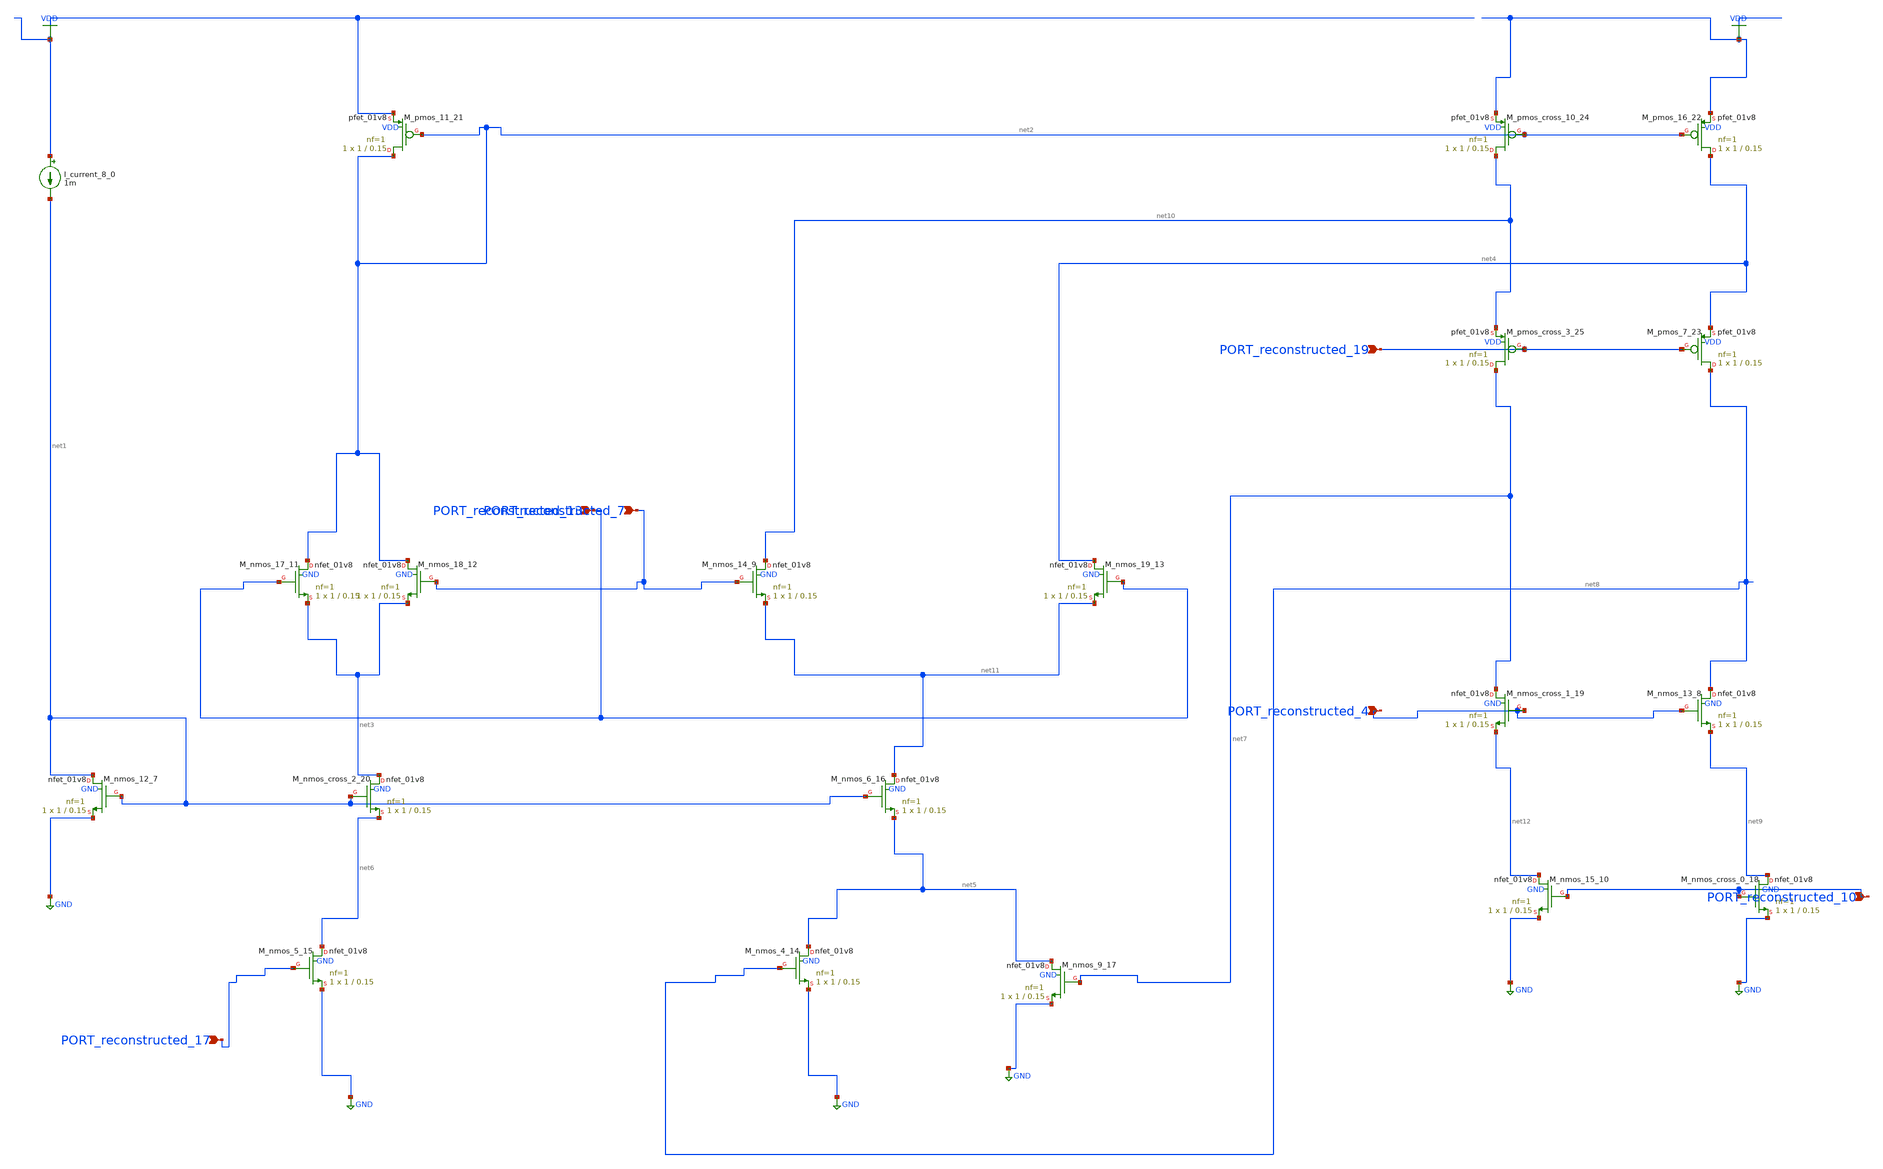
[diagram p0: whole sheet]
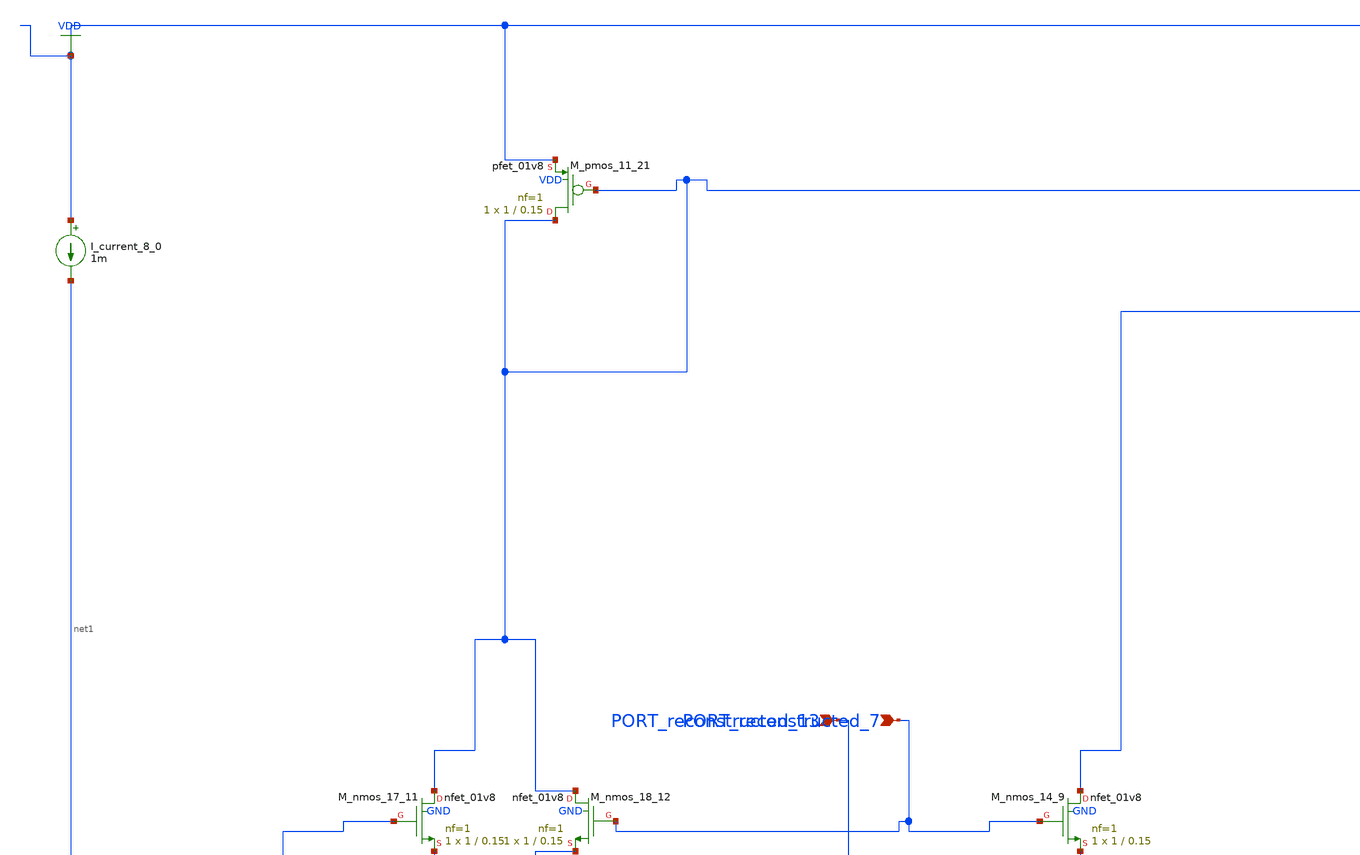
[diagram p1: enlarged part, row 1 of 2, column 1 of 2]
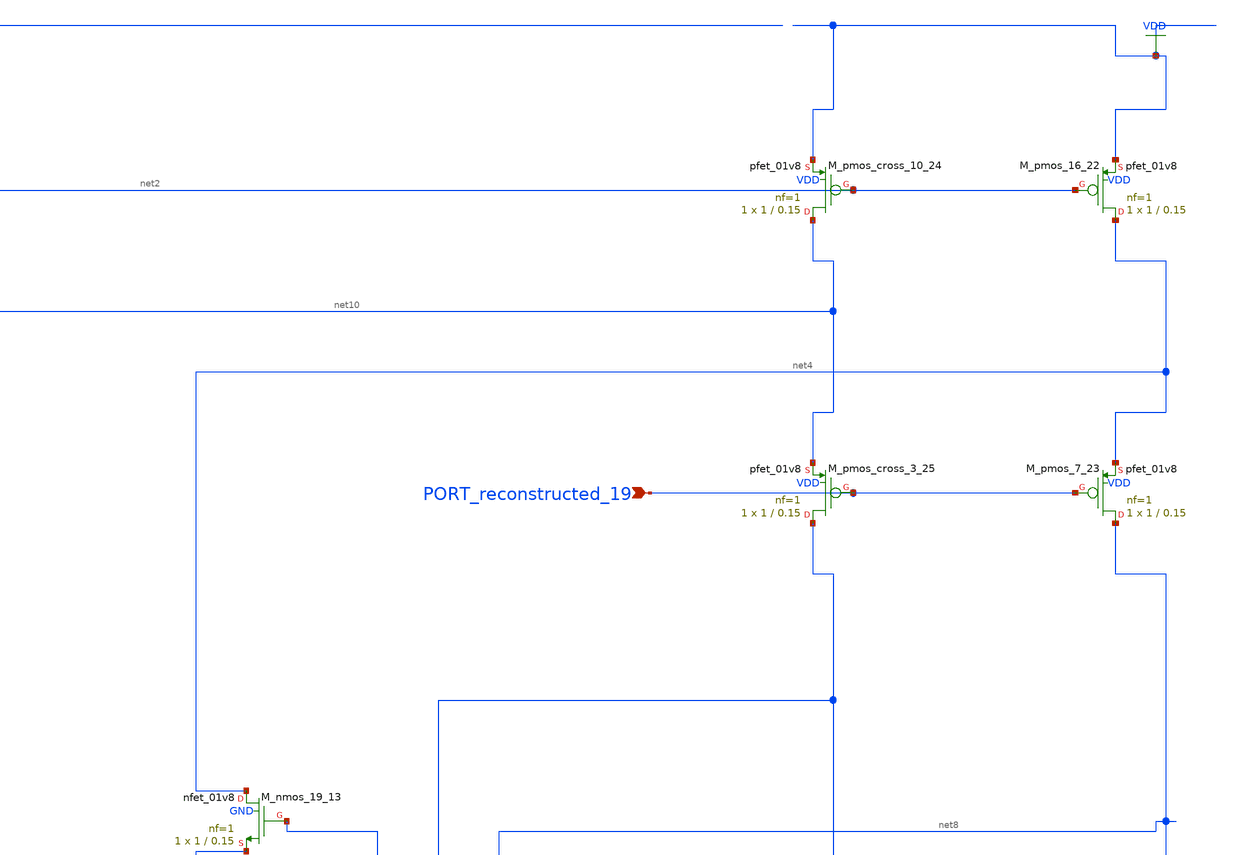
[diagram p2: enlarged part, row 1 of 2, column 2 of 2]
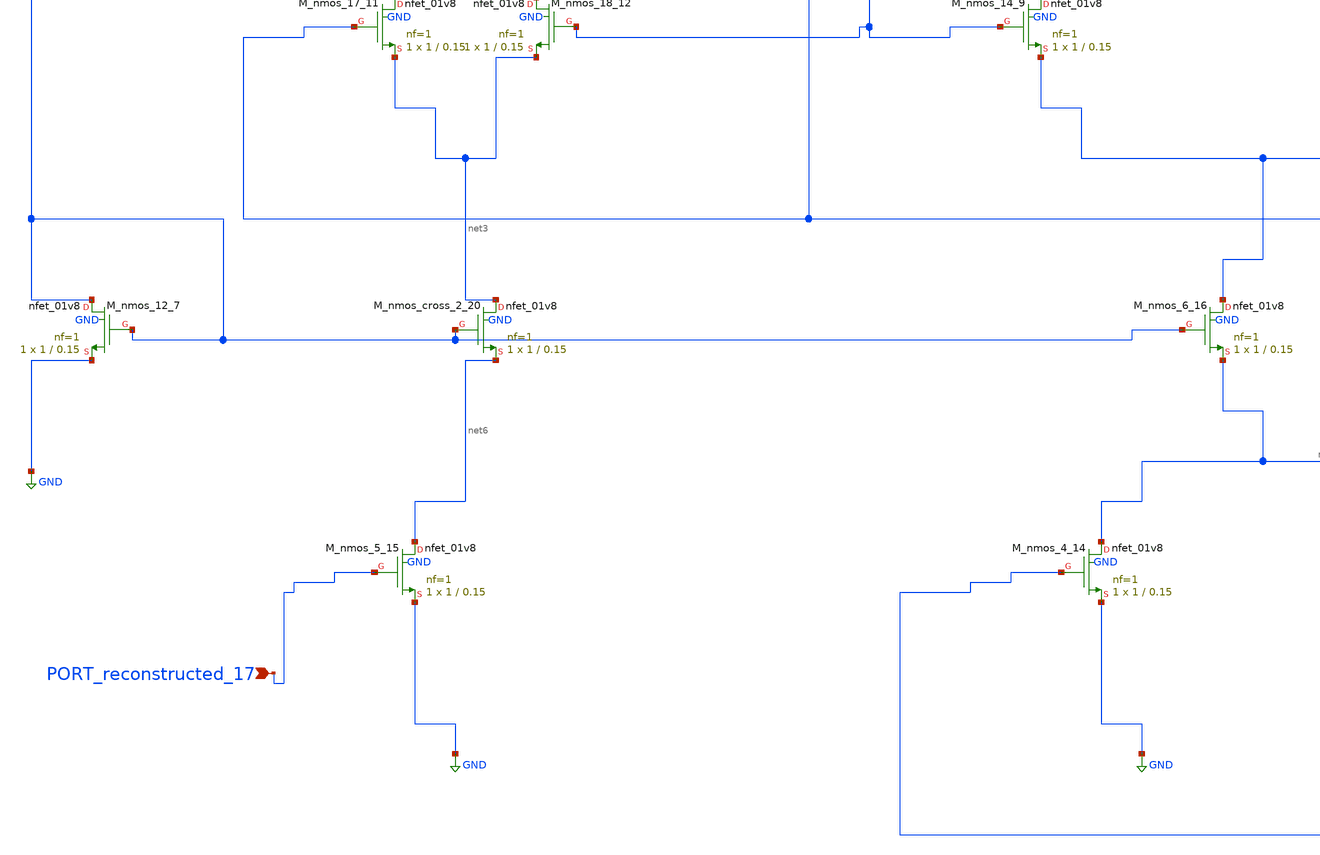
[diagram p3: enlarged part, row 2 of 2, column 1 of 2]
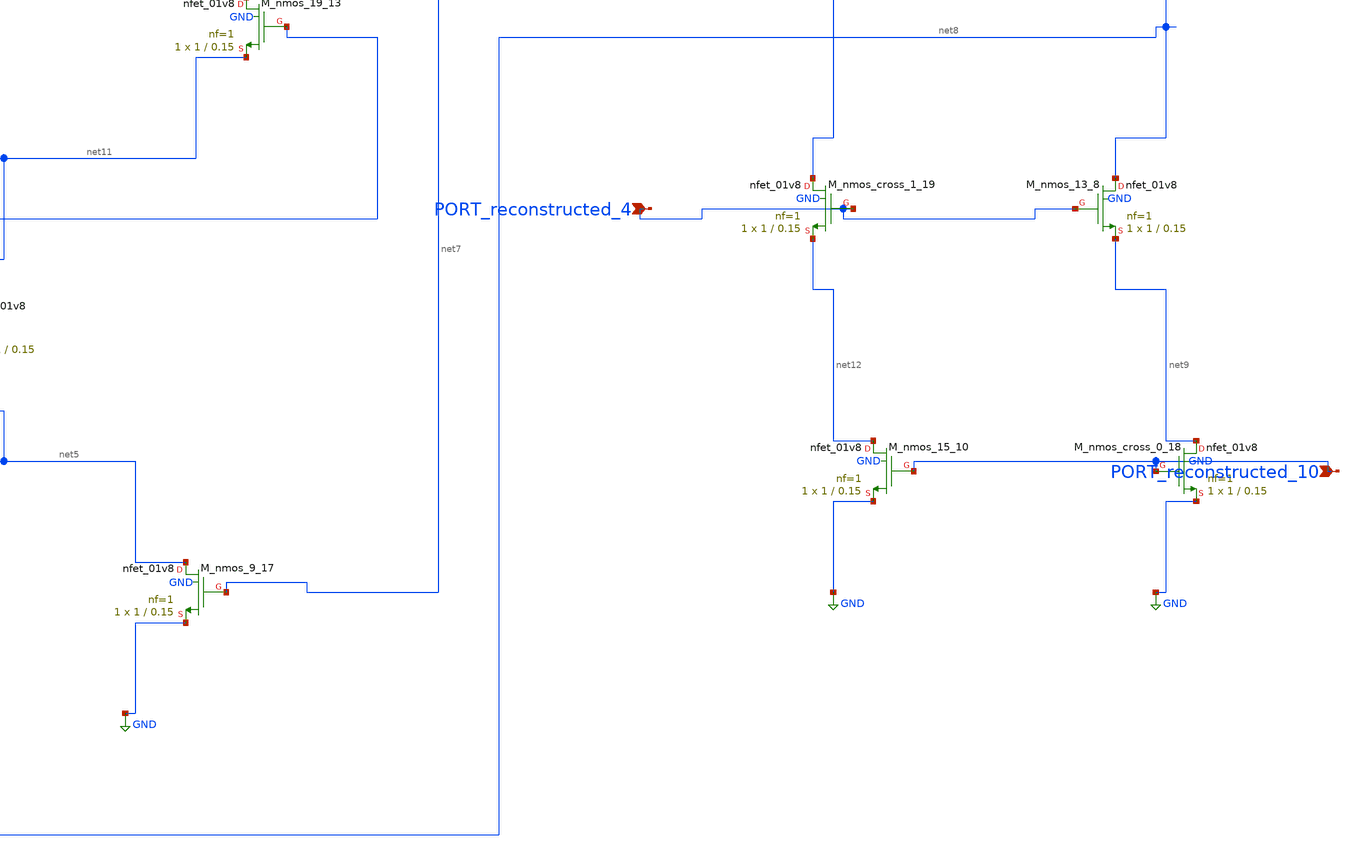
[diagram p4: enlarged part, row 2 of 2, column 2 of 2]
** sch_path: schematics/AMSNet/673.sch
**.subckt 673 PORT_reconstructed_7 PORT_reconstructed_13 PORT_reconstructed_17 PORT_reconstructed_10
*+ PORT_reconstructed_4 PORT_reconstructed_19
*.ipin PORT_reconstructed_7
*.ipin PORT_reconstructed_13
*.ipin PORT_reconstructed_17
*.ipin PORT_reconstructed_10
*.ipin PORT_reconstructed_4
*.ipin PORT_reconstructed_19
I_current_8_0 VDD net1 1m
XM_nmos_12_7 net1 net1 GND GND sky130_fd_pr__nfet_01v8 L=0.15 W=1 nf=1 ad='int((1 + 1)/2) * 1 / 1 * 0.29'
+ as='int((1 + 2)/2) * 1 / 1 * 0.29' pd='2*int((1 + 1)/2) * (1 / 1 + 0.29)' ps='2*int((1 + 2)/2) * (1 / 1 + 0.29)'
+ nrd='0.29 / 1 ' nrs='0.29 / 1 ' sa=0 sb=0 sd=0 mult=1 m=1
XM_nmos_13_8 net8 PORT_reconstructed_4 net9 GND sky130_fd_pr__nfet_01v8 L=0.15 W=1 nf=1 ad='int((1 + 1)/2) * 1 / 1 * 0.29'
+ as='int((1 + 2)/2) * 1 / 1 * 0.29' pd='2*int((1 + 1)/2) * (1 / 1 + 0.29)' ps='2*int((1 + 2)/2) * (1 / 1 + 0.29)'
+ nrd='0.29 / 1 ' nrs='0.29 / 1 ' sa=0 sb=0 sd=0 mult=1 m=1
XM_nmos_14_9 net10 PORT_reconstructed_7 net11 GND sky130_fd_pr__nfet_01v8 L=0.15 W=1 nf=1 ad='int((1 + 1)/2) * 1 / 1 * 0.29'
+ as='int((1 + 2)/2) * 1 / 1 * 0.29' pd='2*int((1 + 1)/2) * (1 / 1 + 0.29)' ps='2*int((1 + 2)/2) * (1 / 1 + 0.29)'
+ nrd='0.29 / 1 ' nrs='0.29 / 1 ' sa=0 sb=0 sd=0 mult=1 m=1
XM_nmos_15_10 net12 PORT_reconstructed_10 GND GND sky130_fd_pr__nfet_01v8 L=0.15 W=1 nf=1 ad='int((1 + 1)/2) * 1 / 1 * 0.29'
+ as='int((1 + 2)/2) * 1 / 1 * 0.29' pd='2*int((1 + 1)/2) * (1 / 1 + 0.29)' ps='2*int((1 + 2)/2) * (1 / 1 + 0.29)'
+ nrd='0.29 / 1 ' nrs='0.29 / 1 ' sa=0 sb=0 sd=0 mult=1 m=1
XM_nmos_17_11 net2 PORT_reconstructed_13 net3 GND sky130_fd_pr__nfet_01v8 L=0.15 W=1 nf=1 ad='int((1 + 1)/2) * 1 / 1 * 0.29'
+ as='int((1 + 2)/2) * 1 / 1 * 0.29' pd='2*int((1 + 1)/2) * (1 / 1 + 0.29)' ps='2*int((1 + 2)/2) * (1 / 1 + 0.29)'
+ nrd='0.29 / 1 ' nrs='0.29 / 1 ' sa=0 sb=0 sd=0 mult=1 m=1
XM_nmos_18_12 net2 PORT_reconstructed_7 net3 GND sky130_fd_pr__nfet_01v8 L=0.15 W=1 nf=1 ad='int((1 + 1)/2) * 1 / 1 * 0.29'
+ as='int((1 + 2)/2) * 1 / 1 * 0.29' pd='2*int((1 + 1)/2) * (1 / 1 + 0.29)' ps='2*int((1 + 2)/2) * (1 / 1 + 0.29)'
+ nrd='0.29 / 1 ' nrs='0.29 / 1 ' sa=0 sb=0 sd=0 mult=1 m=1
XM_nmos_19_13 net4 PORT_reconstructed_13 net11 GND sky130_fd_pr__nfet_01v8 L=0.15 W=1 nf=1 ad='int((1 + 1)/2) * 1 / 1 * 0.29'
+ as='int((1 + 2)/2) * 1 / 1 * 0.29' pd='2*int((1 + 1)/2) * (1 / 1 + 0.29)' ps='2*int((1 + 2)/2) * (1 / 1 + 0.29)'
+ nrd='0.29 / 1 ' nrs='0.29 / 1 ' sa=0 sb=0 sd=0 mult=1 m=1
XM_nmos_4_14 net5 net8 GND GND sky130_fd_pr__nfet_01v8 L=0.15 W=1 nf=1 ad='int((1 + 1)/2) * 1 / 1 * 0.29'
+ as='int((1 + 2)/2) * 1 / 1 * 0.29' pd='2*int((1 + 1)/2) * (1 / 1 + 0.29)' ps='2*int((1 + 2)/2) * (1 / 1 + 0.29)'
+ nrd='0.29 / 1 ' nrs='0.29 / 1 ' sa=0 sb=0 sd=0 mult=1 m=1
XM_nmos_5_15 net6 PORT_reconstructed_17 GND GND sky130_fd_pr__nfet_01v8 L=0.15 W=1 nf=1 ad='int((1 + 1)/2) * 1 / 1 * 0.29'
+ as='int((1 + 2)/2) * 1 / 1 * 0.29' pd='2*int((1 + 1)/2) * (1 / 1 + 0.29)' ps='2*int((1 + 2)/2) * (1 / 1 + 0.29)'
+ nrd='0.29 / 1 ' nrs='0.29 / 1 ' sa=0 sb=0 sd=0 mult=1 m=1
XM_nmos_6_16 net11 net1 net5 GND sky130_fd_pr__nfet_01v8 L=0.15 W=1 nf=1 ad='int((1 + 1)/2) * 1 / 1 * 0.29'
+ as='int((1 + 2)/2) * 1 / 1 * 0.29' pd='2*int((1 + 1)/2) * (1 / 1 + 0.29)' ps='2*int((1 + 2)/2) * (1 / 1 + 0.29)'
+ nrd='0.29 / 1 ' nrs='0.29 / 1 ' sa=0 sb=0 sd=0 mult=1 m=1
XM_nmos_9_17 net5 net7 GND GND sky130_fd_pr__nfet_01v8 L=0.15 W=1 nf=1 ad='int((1 + 1)/2) * 1 / 1 * 0.29'
+ as='int((1 + 2)/2) * 1 / 1 * 0.29' pd='2*int((1 + 1)/2) * (1 / 1 + 0.29)' ps='2*int((1 + 2)/2) * (1 / 1 + 0.29)'
+ nrd='0.29 / 1 ' nrs='0.29 / 1 ' sa=0 sb=0 sd=0 mult=1 m=1
XM_nmos_cross_0_18 net9 PORT_reconstructed_10 GND GND sky130_fd_pr__nfet_01v8 L=0.15 W=1 nf=1 ad='int((1 + 1)/2) * 1 / 1 * 0.29'
+ as='int((1 + 2)/2) * 1 / 1 * 0.29' pd='2*int((1 + 1)/2) * (1 / 1 + 0.29)' ps='2*int((1 + 2)/2) * (1 / 1 + 0.29)'
+ nrd='0.29 / 1 ' nrs='0.29 / 1 ' sa=0 sb=0 sd=0 mult=1 m=1
XM_nmos_cross_1_19 net7 PORT_reconstructed_4 net12 GND sky130_fd_pr__nfet_01v8 L=0.15 W=1 nf=1 ad='int((1 + 1)/2) * 1 / 1 * 0.29'
+ as='int((1 + 2)/2) * 1 / 1 * 0.29' pd='2*int((1 + 1)/2) * (1 / 1 + 0.29)' ps='2*int((1 + 2)/2) * (1 / 1 + 0.29)'
+ nrd='0.29 / 1 ' nrs='0.29 / 1 ' sa=0 sb=0 sd=0 mult=1 m=1
XM_nmos_cross_2_20 net3 net1 net6 GND sky130_fd_pr__nfet_01v8 L=0.15 W=1 nf=1 ad='int((1 + 1)/2) * 1 / 1 * 0.29'
+ as='int((1 + 2)/2) * 1 / 1 * 0.29' pd='2*int((1 + 1)/2) * (1 / 1 + 0.29)' ps='2*int((1 + 2)/2) * (1 / 1 + 0.29)'
+ nrd='0.29 / 1 ' nrs='0.29 / 1 ' sa=0 sb=0 sd=0 mult=1 m=1
XM_pmos_11_21 net2 net2 VDD VDD sky130_fd_pr__pfet_01v8 L=0.15 W=1 nf=1 ad='int((1 + 1)/2) * 1 / 1 * 0.29'
+ as='int((1 + 2)/2) * 1 / 1 * 0.29' pd='2*int((1 + 1)/2) * (1 / 1 + 0.29)' ps='2*int((1 + 2)/2) * (1 / 1 + 0.29)'
+ nrd='0.29 / 1 ' nrs='0.29 / 1 ' sa=0 sb=0 sd=0 mult=1 m=1
XM_pmos_16_22 net4 net2 VDD VDD sky130_fd_pr__pfet_01v8 L=0.15 W=1 nf=1 ad='int((1 + 1)/2) * 1 / 1 * 0.29'
+ as='int((1 + 2)/2) * 1 / 1 * 0.29' pd='2*int((1 + 1)/2) * (1 / 1 + 0.29)' ps='2*int((1 + 2)/2) * (1 / 1 + 0.29)'
+ nrd='0.29 / 1 ' nrs='0.29 / 1 ' sa=0 sb=0 sd=0 mult=1 m=1
XM_pmos_7_23 net8 PORT_reconstructed_19 net4 VDD sky130_fd_pr__pfet_01v8 L=0.15 W=1 nf=1 ad='int((1 + 1)/2) * 1 / 1 * 0.29'
+ as='int((1 + 2)/2) * 1 / 1 * 0.29' pd='2*int((1 + 1)/2) * (1 / 1 + 0.29)' ps='2*int((1 + 2)/2) * (1 / 1 + 0.29)'
+ nrd='0.29 / 1 ' nrs='0.29 / 1 ' sa=0 sb=0 sd=0 mult=1 m=1
XM_pmos_cross_10_24 net10 net2 VDD VDD sky130_fd_pr__pfet_01v8 L=0.15 W=1 nf=1 ad='int((1 + 1)/2) * 1 / 1 * 0.29'
+ as='int((1 + 2)/2) * 1 / 1 * 0.29' pd='2*int((1 + 1)/2) * (1 / 1 + 0.29)' ps='2*int((1 + 2)/2) * (1 / 1 + 0.29)'
+ nrd='0.29 / 1 ' nrs='0.29 / 1 ' sa=0 sb=0 sd=0 mult=1 m=1
XM_pmos_cross_3_25 net7 PORT_reconstructed_19 net10 VDD sky130_fd_pr__pfet_01v8 L=0.15 W=1 nf=1 ad='int((1 + 1)/2) * 1 / 1 * 0.29'
+ as='int((1 + 2)/2) * 1 / 1 * 0.29' pd='2*int((1 + 1)/2) * (1 / 1 + 0.29)' ps='2*int((1 + 2)/2) * (1 / 1 + 0.29)'
+ nrd='0.29 / 1 ' nrs='0.29 / 1 ' sa=0 sb=0 sd=0 mult=1 m=1
**.ends
.GLOBAL GND
.GLOBAL VDD
.end
